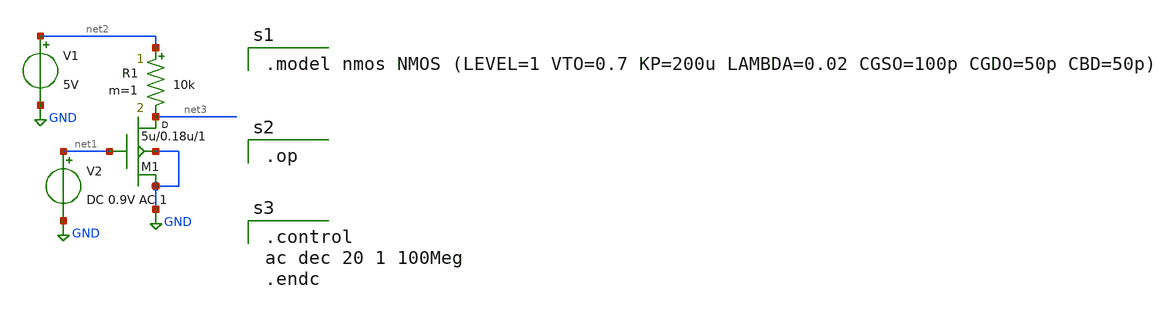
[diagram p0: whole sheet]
** sch_path: schematics/common_source_amp.sch
**.subckt common_source_amp
M1 net3 net1 GND GND nmos w=5u l=0.18u m=1
R1 net2 net3 10k m=1
V1 net2 GND 5V
V2 net1 GND DC 0.9V AC 1
**** begin user architecture code

.model nmos NMOS (LEVEL=1 VTO=0.7 KP=200u LAMBDA=0.02 CGSO=100p CGDO=50p CBD=50p)


.op


.control
ac dec 20 1 100Meg
.endc

**** end user architecture code
**.ends
.GLOBAL GND
.end
